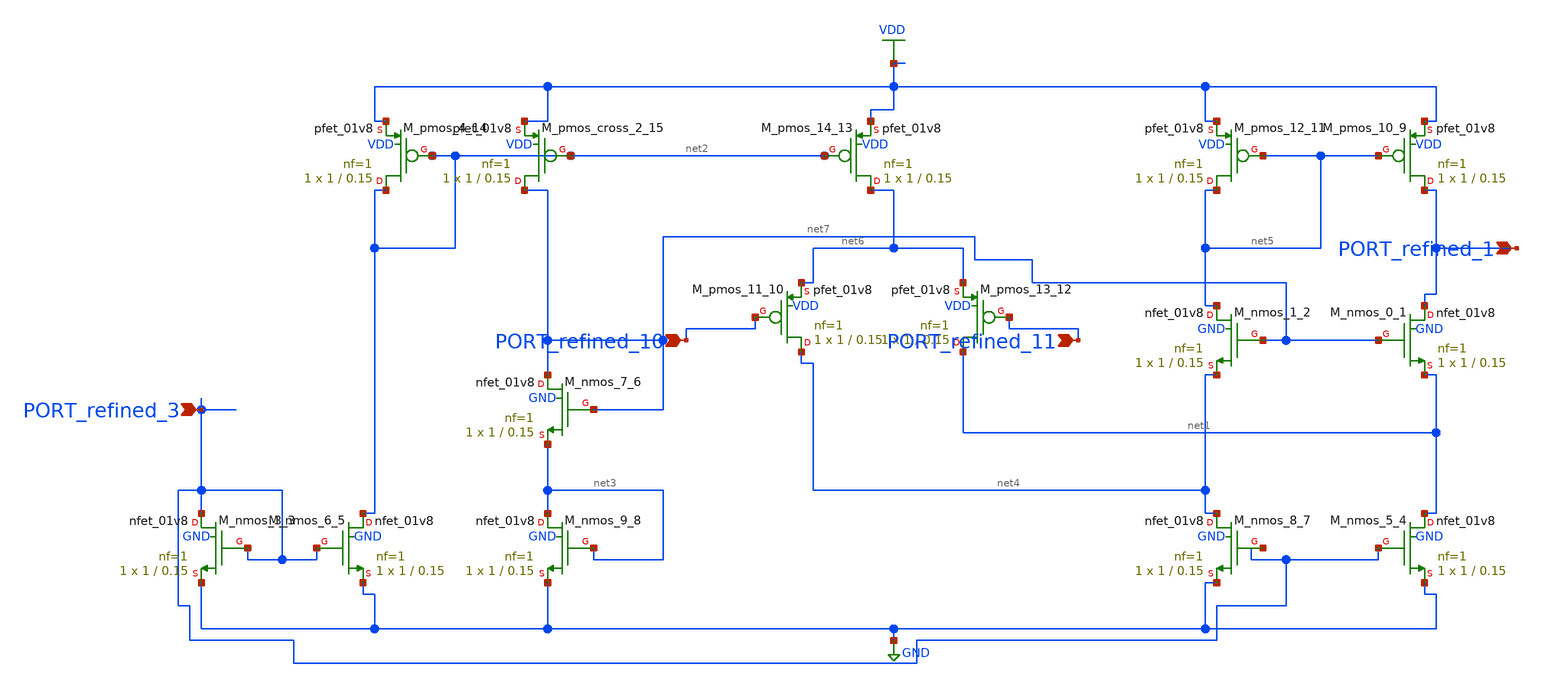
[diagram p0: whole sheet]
** sch_path: schematics/Image2Net/008.sch
**.subckt 008 PORT_refined_1 PORT_refined_11 PORT_refined_10 PORT_refined_3
*.ipin PORT_refined_1
*.ipin PORT_refined_11
*.ipin PORT_refined_10
*.ipin PORT_refined_3
XM_nmos_0_1 PORT_refined_1 net7 net1 GND sky130_fd_pr__nfet_01v8 L=0.15 W=1 nf=1 ad='int((1 + 1)/2) * 1 / 1 * 0.29'
+ as='int((1 + 2)/2) * 1 / 1 * 0.29' pd='2*int((1 + 1)/2) * (1 / 1 + 0.29)' ps='2*int((1 + 2)/2) * (1 / 1 + 0.29)'
+ nrd='0.29 / 1 ' nrs='0.29 / 1 ' sa=0 sb=0 sd=0 mult=1 m=1
XM_nmos_1_2 net5 net7 net4 GND sky130_fd_pr__nfet_01v8 L=0.15 W=1 nf=1 ad='int((1 + 1)/2) * 1 / 1 * 0.29'
+ as='int((1 + 2)/2) * 1 / 1 * 0.29' pd='2*int((1 + 1)/2) * (1 / 1 + 0.29)' ps='2*int((1 + 2)/2) * (1 / 1 + 0.29)'
+ nrd='0.29 / 1 ' nrs='0.29 / 1 ' sa=0 sb=0 sd=0 mult=1 m=1
XM_nmos_3_3 PORT_refined_3 PORT_refined_3 GND GND sky130_fd_pr__nfet_01v8 L=0.15 W=1 nf=1 ad='int((1 + 1)/2) * 1 / 1 * 0.29'
+ as='int((1 + 2)/2) * 1 / 1 * 0.29' pd='2*int((1 + 1)/2) * (1 / 1 + 0.29)' ps='2*int((1 + 2)/2) * (1 / 1 + 0.29)'
+ nrd='0.29 / 1 ' nrs='0.29 / 1 ' sa=0 sb=0 sd=0 mult=1 m=1
XM_nmos_5_4 net1 PORT_refined_3 GND GND sky130_fd_pr__nfet_01v8 L=0.15 W=1 nf=1 ad='int((1 + 1)/2) * 1 / 1 * 0.29'
+ as='int((1 + 2)/2) * 1 / 1 * 0.29' pd='2*int((1 + 1)/2) * (1 / 1 + 0.29)' ps='2*int((1 + 2)/2) * (1 / 1 + 0.29)'
+ nrd='0.29 / 1 ' nrs='0.29 / 1 ' sa=0 sb=0 sd=0 mult=1 m=1
XM_nmos_6_5 net2 PORT_refined_3 GND GND sky130_fd_pr__nfet_01v8 L=0.15 W=1 nf=1 ad='int((1 + 1)/2) * 1 / 1 * 0.29'
+ as='int((1 + 2)/2) * 1 / 1 * 0.29' pd='2*int((1 + 1)/2) * (1 / 1 + 0.29)' ps='2*int((1 + 2)/2) * (1 / 1 + 0.29)'
+ nrd='0.29 / 1 ' nrs='0.29 / 1 ' sa=0 sb=0 sd=0 mult=1 m=1
XM_nmos_7_6 net7 net7 net3 GND sky130_fd_pr__nfet_01v8 L=0.15 W=1 nf=1 ad='int((1 + 1)/2) * 1 / 1 * 0.29'
+ as='int((1 + 2)/2) * 1 / 1 * 0.29' pd='2*int((1 + 1)/2) * (1 / 1 + 0.29)' ps='2*int((1 + 2)/2) * (1 / 1 + 0.29)'
+ nrd='0.29 / 1 ' nrs='0.29 / 1 ' sa=0 sb=0 sd=0 mult=1 m=1
XM_nmos_8_7 net4 PORT_refined_3 GND GND sky130_fd_pr__nfet_01v8 L=0.15 W=1 nf=1 ad='int((1 + 1)/2) * 1 / 1 * 0.29'
+ as='int((1 + 2)/2) * 1 / 1 * 0.29' pd='2*int((1 + 1)/2) * (1 / 1 + 0.29)' ps='2*int((1 + 2)/2) * (1 / 1 + 0.29)'
+ nrd='0.29 / 1 ' nrs='0.29 / 1 ' sa=0 sb=0 sd=0 mult=1 m=1
XM_nmos_9_8 net3 net3 GND GND sky130_fd_pr__nfet_01v8 L=0.15 W=1 nf=1 ad='int((1 + 1)/2) * 1 / 1 * 0.29'
+ as='int((1 + 2)/2) * 1 / 1 * 0.29' pd='2*int((1 + 1)/2) * (1 / 1 + 0.29)' ps='2*int((1 + 2)/2) * (1 / 1 + 0.29)'
+ nrd='0.29 / 1 ' nrs='0.29 / 1 ' sa=0 sb=0 sd=0 mult=1 m=1
XM_pmos_10_9 PORT_refined_1 net5 VDD VDD sky130_fd_pr__pfet_01v8 L=0.15 W=1 nf=1 ad='int((1 + 1)/2) * 1 / 1 * 0.29'
+ as='int((1 + 2)/2) * 1 / 1 * 0.29' pd='2*int((1 + 1)/2) * (1 / 1 + 0.29)' ps='2*int((1 + 2)/2) * (1 / 1 + 0.29)'
+ nrd='0.29 / 1 ' nrs='0.29 / 1 ' sa=0 sb=0 sd=0 mult=1 m=1
XM_pmos_11_10 net4 PORT_refined_10 net6 VDD sky130_fd_pr__pfet_01v8 L=0.15 W=1 nf=1 ad='int((1 + 1)/2) * 1 / 1 * 0.29'
+ as='int((1 + 2)/2) * 1 / 1 * 0.29' pd='2*int((1 + 1)/2) * (1 / 1 + 0.29)' ps='2*int((1 + 2)/2) * (1 / 1 + 0.29)'
+ nrd='0.29 / 1 ' nrs='0.29 / 1 ' sa=0 sb=0 sd=0 mult=1 m=1
XM_pmos_12_11 net5 net5 VDD VDD sky130_fd_pr__pfet_01v8 L=0.15 W=1 nf=1 ad='int((1 + 1)/2) * 1 / 1 * 0.29'
+ as='int((1 + 2)/2) * 1 / 1 * 0.29' pd='2*int((1 + 1)/2) * (1 / 1 + 0.29)' ps='2*int((1 + 2)/2) * (1 / 1 + 0.29)'
+ nrd='0.29 / 1 ' nrs='0.29 / 1 ' sa=0 sb=0 sd=0 mult=1 m=1
XM_pmos_13_12 net1 PORT_refined_11 net6 VDD sky130_fd_pr__pfet_01v8 L=0.15 W=1 nf=1 ad='int((1 + 1)/2) * 1 / 1 * 0.29'
+ as='int((1 + 2)/2) * 1 / 1 * 0.29' pd='2*int((1 + 1)/2) * (1 / 1 + 0.29)' ps='2*int((1 + 2)/2) * (1 / 1 + 0.29)'
+ nrd='0.29 / 1 ' nrs='0.29 / 1 ' sa=0 sb=0 sd=0 mult=1 m=1
XM_pmos_14_13 net6 net2 VDD VDD sky130_fd_pr__pfet_01v8 L=0.15 W=1 nf=1 ad='int((1 + 1)/2) * 1 / 1 * 0.29'
+ as='int((1 + 2)/2) * 1 / 1 * 0.29' pd='2*int((1 + 1)/2) * (1 / 1 + 0.29)' ps='2*int((1 + 2)/2) * (1 / 1 + 0.29)'
+ nrd='0.29 / 1 ' nrs='0.29 / 1 ' sa=0 sb=0 sd=0 mult=1 m=1
XM_pmos_4_14 net2 net2 VDD VDD sky130_fd_pr__pfet_01v8 L=0.15 W=1 nf=1 ad='int((1 + 1)/2) * 1 / 1 * 0.29'
+ as='int((1 + 2)/2) * 1 / 1 * 0.29' pd='2*int((1 + 1)/2) * (1 / 1 + 0.29)' ps='2*int((1 + 2)/2) * (1 / 1 + 0.29)'
+ nrd='0.29 / 1 ' nrs='0.29 / 1 ' sa=0 sb=0 sd=0 mult=1 m=1
XM_pmos_cross_2_15 net7 net2 VDD VDD sky130_fd_pr__pfet_01v8 L=0.15 W=1 nf=1 ad='int((1 + 1)/2) * 1 / 1 * 0.29'
+ as='int((1 + 2)/2) * 1 / 1 * 0.29' pd='2*int((1 + 1)/2) * (1 / 1 + 0.29)' ps='2*int((1 + 2)/2) * (1 / 1 + 0.29)'
+ nrd='0.29 / 1 ' nrs='0.29 / 1 ' sa=0 sb=0 sd=0 mult=1 m=1
**.ends
.GLOBAL GND
.GLOBAL VDD
.end
